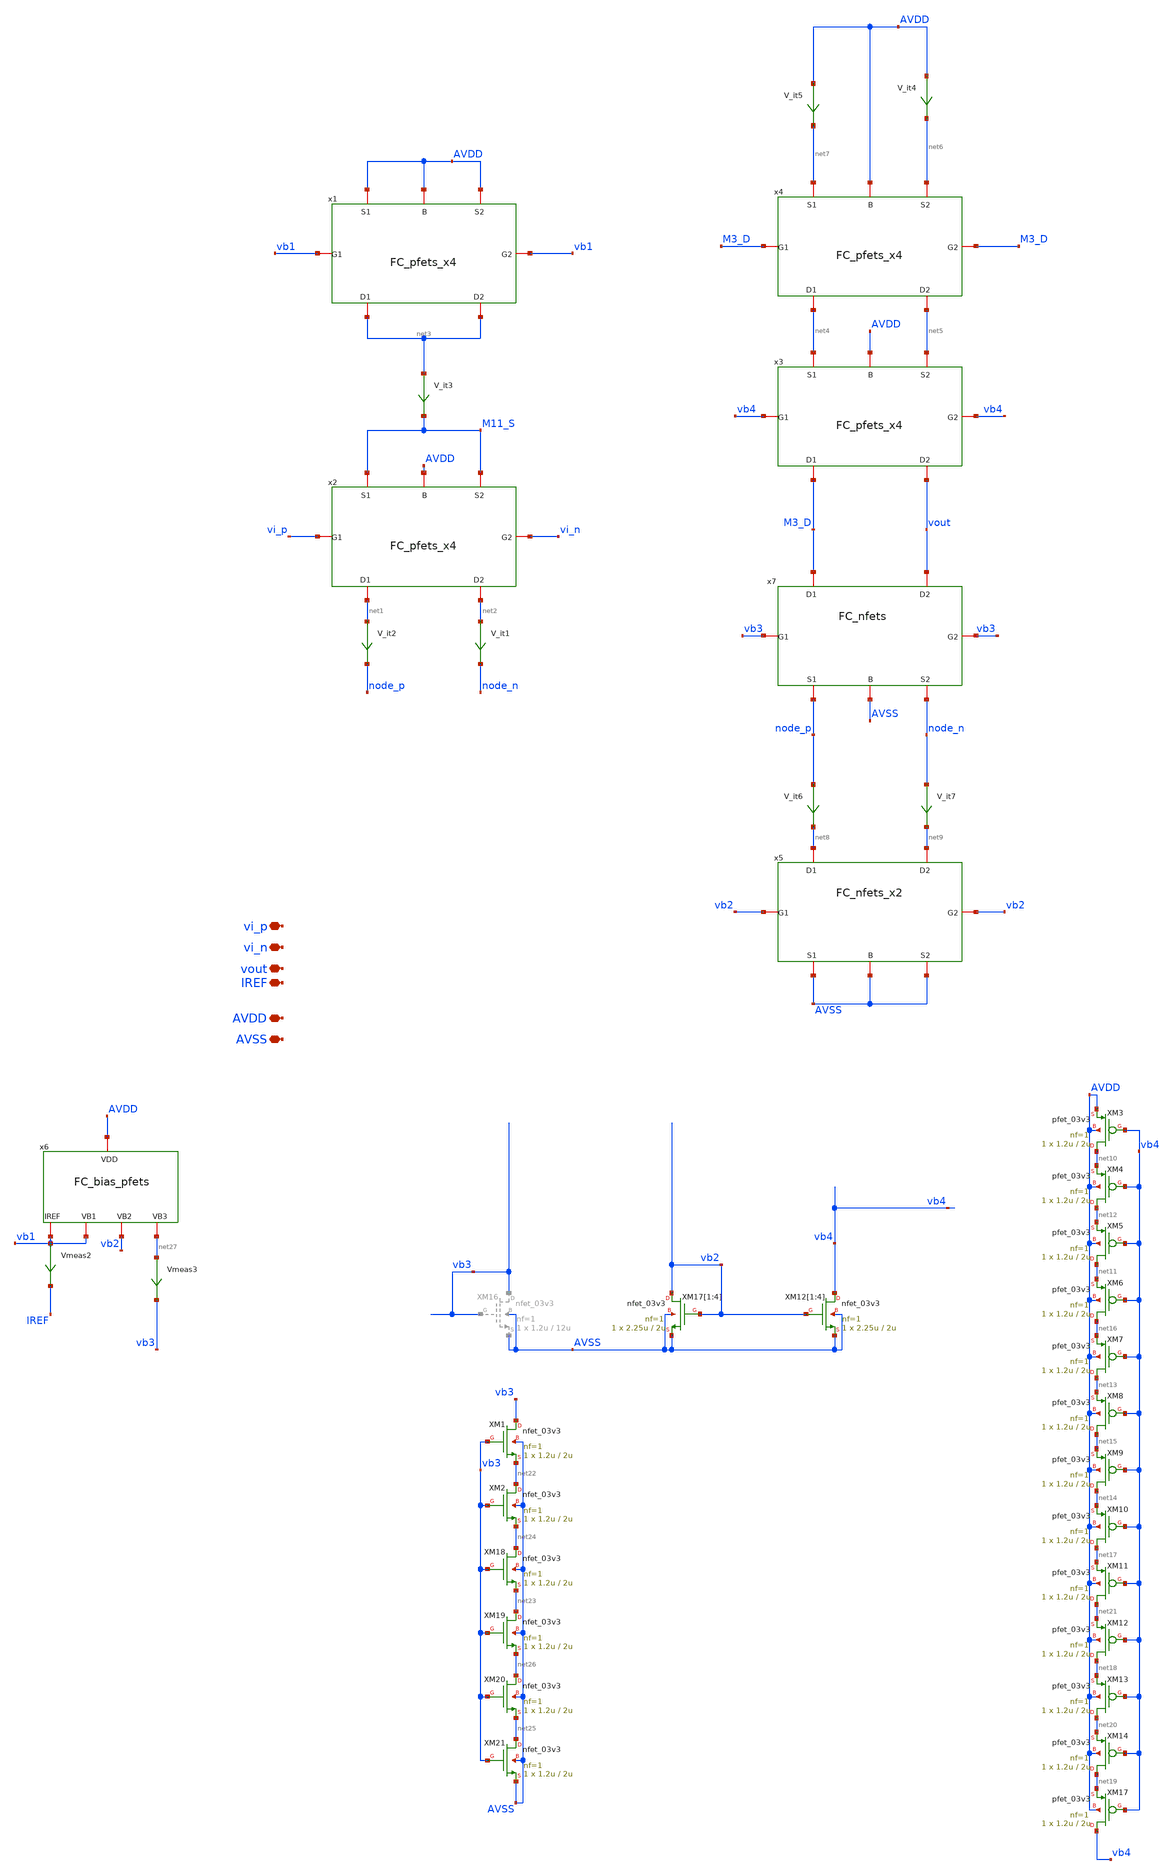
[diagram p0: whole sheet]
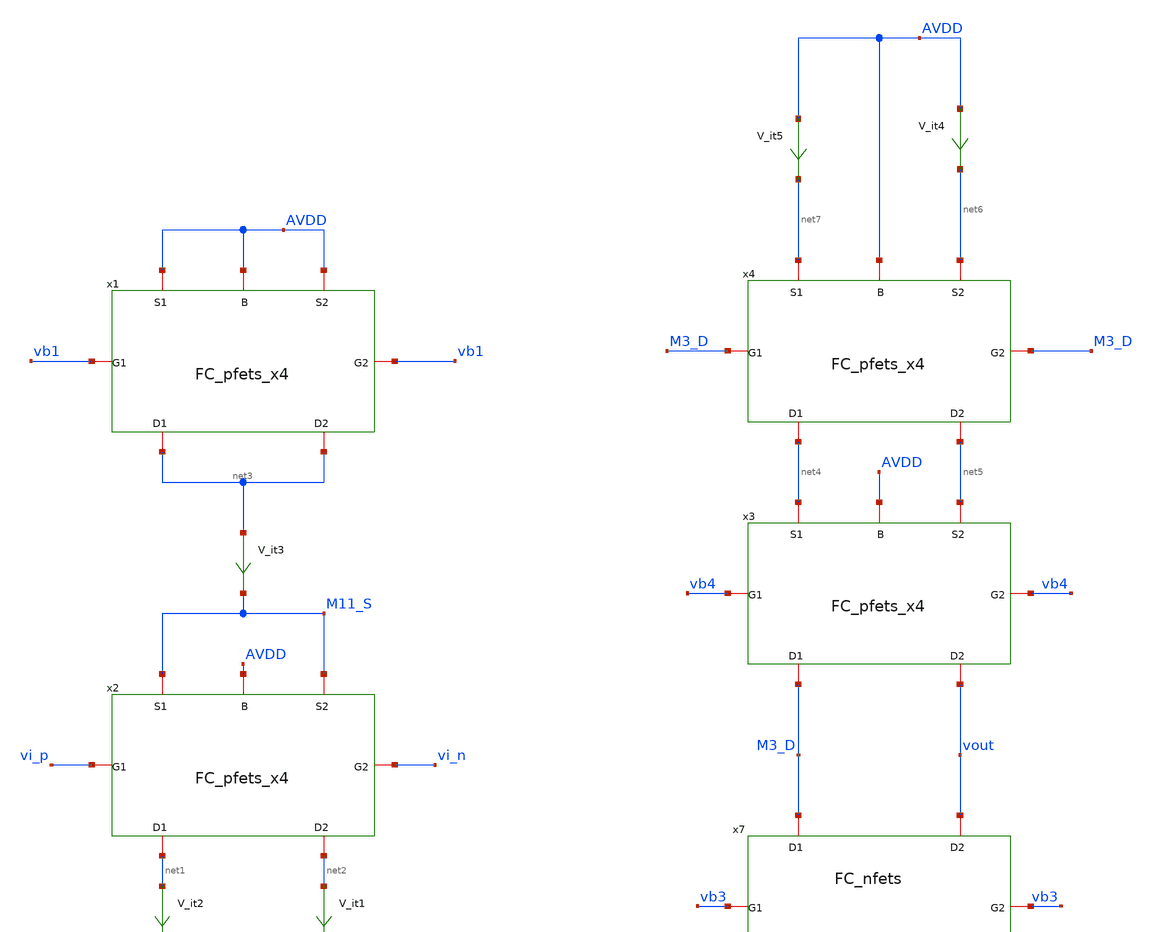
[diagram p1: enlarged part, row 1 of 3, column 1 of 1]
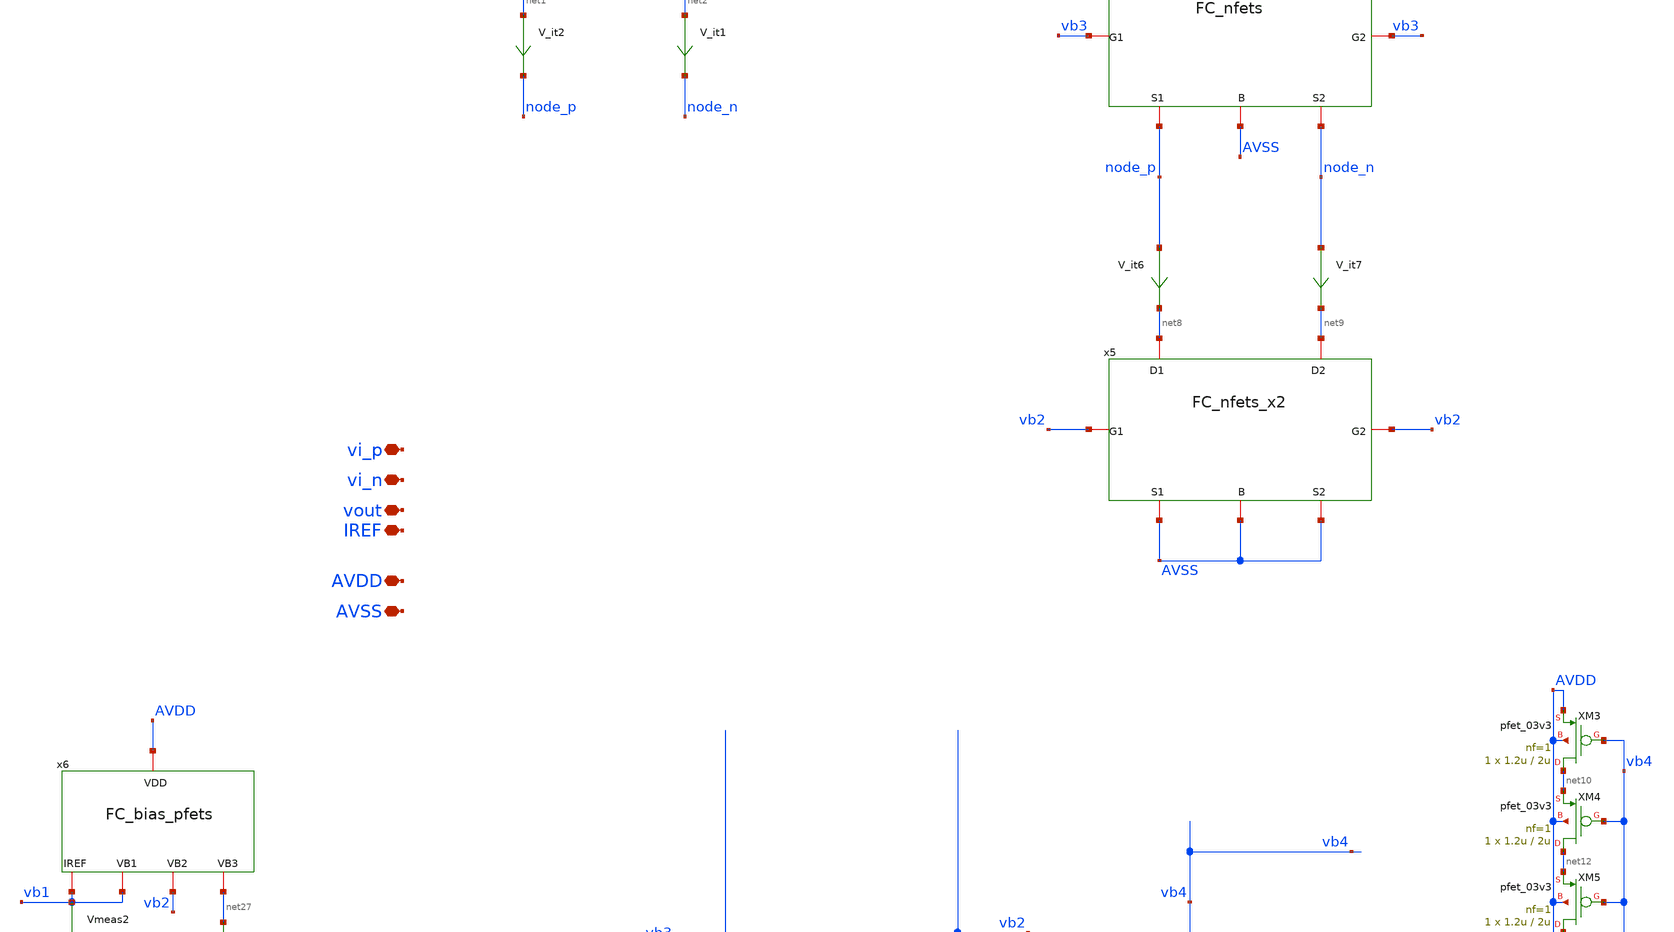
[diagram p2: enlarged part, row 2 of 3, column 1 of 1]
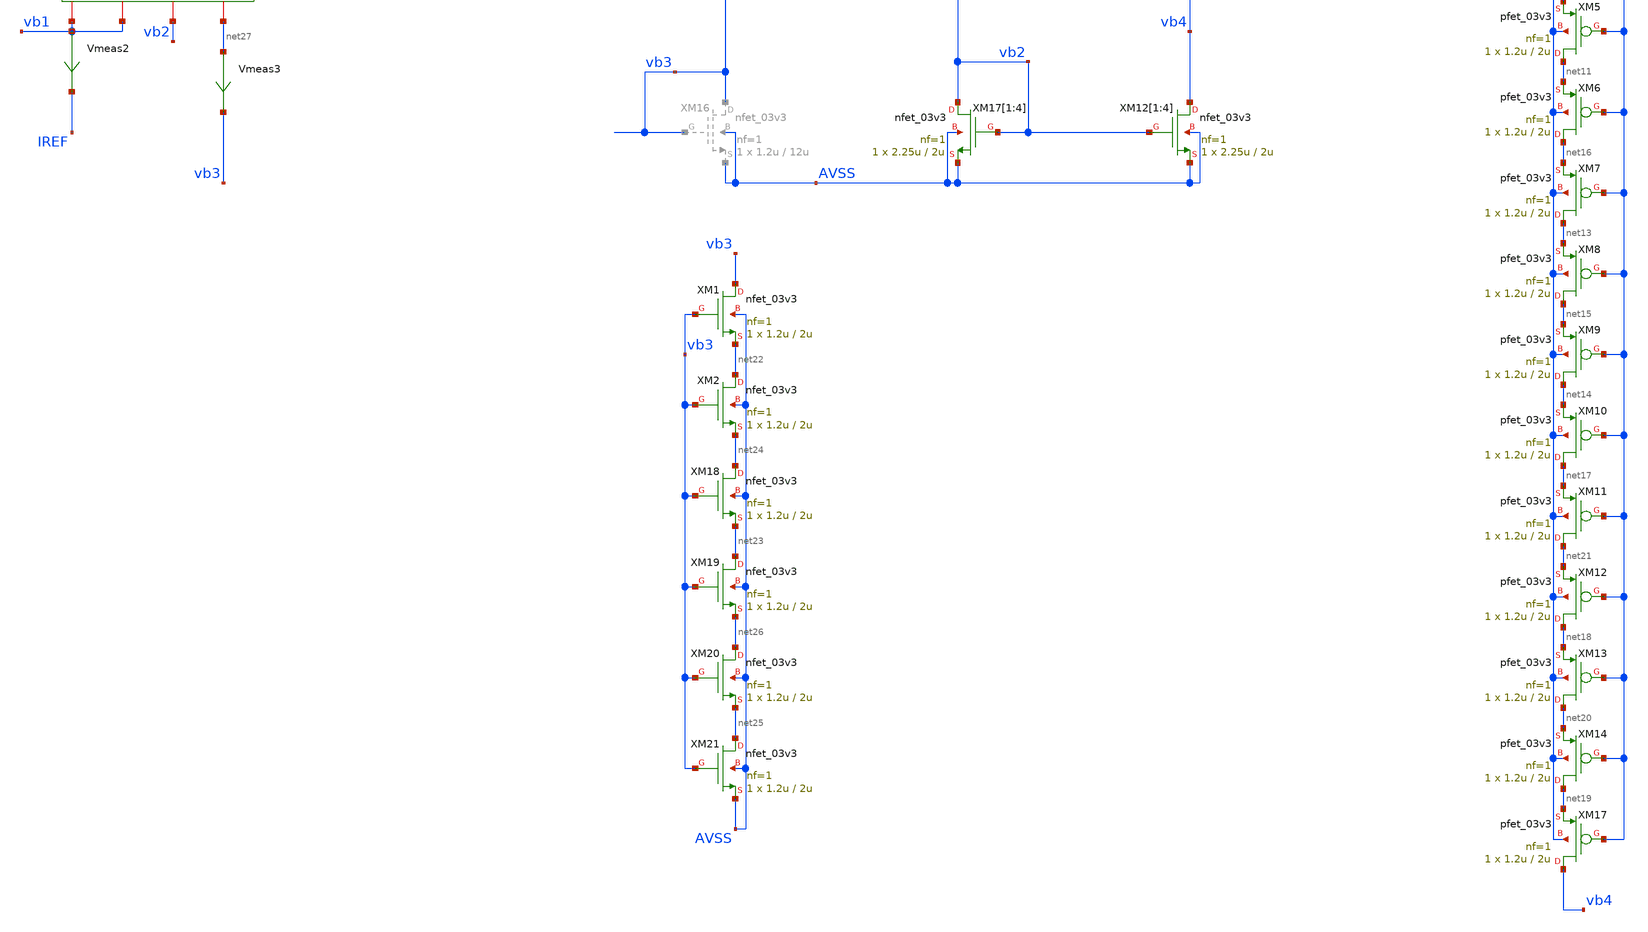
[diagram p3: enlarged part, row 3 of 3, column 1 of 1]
** sch_path: TIA_Filter/Folded/FoldedCascode.sch
**.subckt FoldedCascode AVDD AVSS vout vi_p vi_n IREF
*.iopin AVDD
*.iopin AVSS
*.iopin vout
*.iopin vi_p
*.iopin vi_n
*.iopin IREF
XM17[1] vb2 vb2 AVSS AVSS nfet_03v3 L=2u W=2.25u nf=1 ad='int((nf+1)/2) * W/nf * 0.18u' as='int((nf+2)/2) * W/nf * 0.18u'
+ pd='2*int((nf+1)/2) * (W/nf + 0.18u)' ps='2*int((nf+2)/2) * (W/nf + 0.18u)' nrd='0.18u / W' nrs='0.18u / W'
+ sa=0 sb=0 sd=0 m=1
XM17[2] vb2 vb2 AVSS AVSS nfet_03v3 L=2u W=2.25u nf=1 ad='int((nf+1)/2) * W/nf * 0.18u' as='int((nf+2)/2) * W/nf * 0.18u'
+ pd='2*int((nf+1)/2) * (W/nf + 0.18u)' ps='2*int((nf+2)/2) * (W/nf + 0.18u)' nrd='0.18u / W' nrs='0.18u / W'
+ sa=0 sb=0 sd=0 m=1
XM17[3] vb2 vb2 AVSS AVSS nfet_03v3 L=2u W=2.25u nf=1 ad='int((nf+1)/2) * W/nf * 0.18u' as='int((nf+2)/2) * W/nf * 0.18u'
+ pd='2*int((nf+1)/2) * (W/nf + 0.18u)' ps='2*int((nf+2)/2) * (W/nf + 0.18u)' nrd='0.18u / W' nrs='0.18u / W'
+ sa=0 sb=0 sd=0 m=1
XM17[4] vb2 vb2 AVSS AVSS nfet_03v3 L=2u W=2.25u nf=1 ad='int((nf+1)/2) * W/nf * 0.18u' as='int((nf+2)/2) * W/nf * 0.18u'
+ pd='2*int((nf+1)/2) * (W/nf + 0.18u)' ps='2*int((nf+2)/2) * (W/nf + 0.18u)' nrd='0.18u / W' nrs='0.18u / W'
+ sa=0 sb=0 sd=0 m=1
XM12[1] vb4 vb2 AVSS AVSS nfet_03v3 L=2u W=2.25u nf=1 ad='int((nf+1)/2) * W/nf * 0.18u' as='int((nf+2)/2) * W/nf * 0.18u'
+ pd='2*int((nf+1)/2) * (W/nf + 0.18u)' ps='2*int((nf+2)/2) * (W/nf + 0.18u)' nrd='0.18u / W' nrs='0.18u / W'
+ sa=0 sb=0 sd=0 m=1
XM12[2] vb4 vb2 AVSS AVSS nfet_03v3 L=2u W=2.25u nf=1 ad='int((nf+1)/2) * W/nf * 0.18u' as='int((nf+2)/2) * W/nf * 0.18u'
+ pd='2*int((nf+1)/2) * (W/nf + 0.18u)' ps='2*int((nf+2)/2) * (W/nf + 0.18u)' nrd='0.18u / W' nrs='0.18u / W'
+ sa=0 sb=0 sd=0 m=1
XM12[3] vb4 vb2 AVSS AVSS nfet_03v3 L=2u W=2.25u nf=1 ad='int((nf+1)/2) * W/nf * 0.18u' as='int((nf+2)/2) * W/nf * 0.18u'
+ pd='2*int((nf+1)/2) * (W/nf + 0.18u)' ps='2*int((nf+2)/2) * (W/nf + 0.18u)' nrd='0.18u / W' nrs='0.18u / W'
+ sa=0 sb=0 sd=0 m=1
XM12[4] vb4 vb2 AVSS AVSS nfet_03v3 L=2u W=2.25u nf=1 ad='int((nf+1)/2) * W/nf * 0.18u' as='int((nf+2)/2) * W/nf * 0.18u'
+ pd='2*int((nf+1)/2) * (W/nf + 0.18u)' ps='2*int((nf+2)/2) * (W/nf + 0.18u)' nrd='0.18u / W' nrs='0.18u / W'
+ sa=0 sb=0 sd=0 m=1
V_it1 net2 node_n 0
.save i(v_it1)
V_it2 net1 node_p 0
.save i(v_it2)
V_it3 net3 M11_S 0
.save i(v_it3)
V_it4 AVDD net6 0
.save i(v_it4)
V_it5 AVDD net7 0
.save i(v_it5)
V_it6 node_p net8 0
.save i(v_it6)
V_it7 node_n net9 0
.save i(v_it7)
x7 node_p node_n M3_D vout vb3 vb3 AVSS FC_nfets
x5 AVSS AVSS net8 net9 vb2 vb2 AVSS FC_nfets_x2
x1 AVDD AVDD net3 net3 vb1 vb1 AVDD FC_pfets_x4
x2 M11_S M11_S net1 net2 vi_p vi_n AVDD FC_pfets_x4
x3 net4 net5 M3_D vout vb4 vb4 AVDD FC_pfets_x4
x4 net7 net6 net4 net5 M3_D M3_D AVDD FC_pfets_x4
XM3 net10 vb4 AVDD AVDD pfet_03v3 L=2u W=1.2u nf=1 ad='int((nf+1)/2) * W/nf * 0.18u' as='int((nf+2)/2) * W/nf * 0.18u'
+ pd='2*int((nf+1)/2) * (W/nf + 0.18u)' ps='2*int((nf+2)/2) * (W/nf + 0.18u)' nrd='0.18u / W' nrs='0.18u / W'
+ sa=0 sb=0 sd=0 m=1
XM4 net12 vb4 net10 AVDD pfet_03v3 L=2u W=1.2u nf=1 ad='int((nf+1)/2) * W/nf * 0.18u' as='int((nf+2)/2) * W/nf * 0.18u'
+ pd='2*int((nf+1)/2) * (W/nf + 0.18u)' ps='2*int((nf+2)/2) * (W/nf + 0.18u)' nrd='0.18u / W' nrs='0.18u / W'
+ sa=0 sb=0 sd=0 m=1
XM5 net11 vb4 net12 AVDD pfet_03v3 L=2u W=1.2u nf=1 ad='int((nf+1)/2) * W/nf * 0.18u' as='int((nf+2)/2) * W/nf * 0.18u'
+ pd='2*int((nf+1)/2) * (W/nf + 0.18u)' ps='2*int((nf+2)/2) * (W/nf + 0.18u)' nrd='0.18u / W' nrs='0.18u / W'
+ sa=0 sb=0 sd=0 m=1
XM6 net16 vb4 net11 AVDD pfet_03v3 L=2u W=1.2u nf=1 ad='int((nf+1)/2) * W/nf * 0.18u' as='int((nf+2)/2) * W/nf * 0.18u'
+ pd='2*int((nf+1)/2) * (W/nf + 0.18u)' ps='2*int((nf+2)/2) * (W/nf + 0.18u)' nrd='0.18u / W' nrs='0.18u / W'
+ sa=0 sb=0 sd=0 m=1
XM7 net13 vb4 net16 AVDD pfet_03v3 L=2u W=1.2u nf=1 ad='int((nf+1)/2) * W/nf * 0.18u' as='int((nf+2)/2) * W/nf * 0.18u'
+ pd='2*int((nf+1)/2) * (W/nf + 0.18u)' ps='2*int((nf+2)/2) * (W/nf + 0.18u)' nrd='0.18u / W' nrs='0.18u / W'
+ sa=0 sb=0 sd=0 m=1
XM8 net15 vb4 net13 AVDD pfet_03v3 L=2u W=1.2u nf=1 ad='int((nf+1)/2) * W/nf * 0.18u' as='int((nf+2)/2) * W/nf * 0.18u'
+ pd='2*int((nf+1)/2) * (W/nf + 0.18u)' ps='2*int((nf+2)/2) * (W/nf + 0.18u)' nrd='0.18u / W' nrs='0.18u / W'
+ sa=0 sb=0 sd=0 m=1
XM9 net14 vb4 net15 AVDD pfet_03v3 L=2u W=1.2u nf=1 ad='int((nf+1)/2) * W/nf * 0.18u' as='int((nf+2)/2) * W/nf * 0.18u'
+ pd='2*int((nf+1)/2) * (W/nf + 0.18u)' ps='2*int((nf+2)/2) * (W/nf + 0.18u)' nrd='0.18u / W' nrs='0.18u / W'
+ sa=0 sb=0 sd=0 m=1
XM10 net17 vb4 net14 AVDD pfet_03v3 L=2u W=1.2u nf=1 ad='int((nf+1)/2) * W/nf * 0.18u' as='int((nf+2)/2) * W/nf * 0.18u'
+ pd='2*int((nf+1)/2) * (W/nf + 0.18u)' ps='2*int((nf+2)/2) * (W/nf + 0.18u)' nrd='0.18u / W' nrs='0.18u / W'
+ sa=0 sb=0 sd=0 m=1
XM11 net21 vb4 net17 AVDD pfet_03v3 L=2u W=1.2u nf=1 ad='int((nf+1)/2) * W/nf * 0.18u' as='int((nf+2)/2) * W/nf * 0.18u'
+ pd='2*int((nf+1)/2) * (W/nf + 0.18u)' ps='2*int((nf+2)/2) * (W/nf + 0.18u)' nrd='0.18u / W' nrs='0.18u / W'
+ sa=0 sb=0 sd=0 m=1
XM12 net18 vb4 net21 AVDD pfet_03v3 L=2u W=1.2u nf=1 ad='int((nf+1)/2) * W/nf * 0.18u' as='int((nf+2)/2) * W/nf * 0.18u'
+ pd='2*int((nf+1)/2) * (W/nf + 0.18u)' ps='2*int((nf+2)/2) * (W/nf + 0.18u)' nrd='0.18u / W' nrs='0.18u / W'
+ sa=0 sb=0 sd=0 m=1
XM13 net20 vb4 net18 AVDD pfet_03v3 L=2u W=1.2u nf=1 ad='int((nf+1)/2) * W/nf * 0.18u' as='int((nf+2)/2) * W/nf * 0.18u'
+ pd='2*int((nf+1)/2) * (W/nf + 0.18u)' ps='2*int((nf+2)/2) * (W/nf + 0.18u)' nrd='0.18u / W' nrs='0.18u / W'
+ sa=0 sb=0 sd=0 m=1
XM14 net19 vb4 net20 AVDD pfet_03v3 L=2u W=1.2u nf=1 ad='int((nf+1)/2) * W/nf * 0.18u' as='int((nf+2)/2) * W/nf * 0.18u'
+ pd='2*int((nf+1)/2) * (W/nf + 0.18u)' ps='2*int((nf+2)/2) * (W/nf + 0.18u)' nrd='0.18u / W' nrs='0.18u / W'
+ sa=0 sb=0 sd=0 m=1
XM17 vb4 vb4 net19 AVDD pfet_03v3 L=2u W=1.2u nf=1 ad='int((nf+1)/2) * W/nf * 0.18u' as='int((nf+2)/2) * W/nf * 0.18u'
+ pd='2*int((nf+1)/2) * (W/nf + 0.18u)' ps='2*int((nf+2)/2) * (W/nf + 0.18u)' nrd='0.18u / W' nrs='0.18u / W'
+ sa=0 sb=0 sd=0 m=1
XM1 vb3 vb3 net22 AVSS nfet_03v3 L=2u W=1.2u nf=1 ad='int((nf+1)/2) * W/nf * 0.18u' as='int((nf+2)/2) * W/nf * 0.18u'
+ pd='2*int((nf+1)/2) * (W/nf + 0.18u)' ps='2*int((nf+2)/2) * (W/nf + 0.18u)' nrd='0.18u / W' nrs='0.18u / W'
+ sa=0 sb=0 sd=0 m=1
XM2 net22 vb3 net24 AVSS nfet_03v3 L=2u W=1.2u nf=1 ad='int((nf+1)/2) * W/nf * 0.18u' as='int((nf+2)/2) * W/nf * 0.18u'
+ pd='2*int((nf+1)/2) * (W/nf + 0.18u)' ps='2*int((nf+2)/2) * (W/nf + 0.18u)' nrd='0.18u / W' nrs='0.18u / W'
+ sa=0 sb=0 sd=0 m=1
XM18 net24 vb3 net23 AVSS nfet_03v3 L=2u W=1.2u nf=1 ad='int((nf+1)/2) * W/nf * 0.18u' as='int((nf+2)/2) * W/nf * 0.18u'
+ pd='2*int((nf+1)/2) * (W/nf + 0.18u)' ps='2*int((nf+2)/2) * (W/nf + 0.18u)' nrd='0.18u / W' nrs='0.18u / W'
+ sa=0 sb=0 sd=0 m=1
XM19 net23 vb3 net26 AVSS nfet_03v3 L=2u W=1.2u nf=1 ad='int((nf+1)/2) * W/nf * 0.18u' as='int((nf+2)/2) * W/nf * 0.18u'
+ pd='2*int((nf+1)/2) * (W/nf + 0.18u)' ps='2*int((nf+2)/2) * (W/nf + 0.18u)' nrd='0.18u / W' nrs='0.18u / W'
+ sa=0 sb=0 sd=0 m=1
XM20 net26 vb3 net25 AVSS nfet_03v3 L=2u W=1.2u nf=1 ad='int((nf+1)/2) * W/nf * 0.18u' as='int((nf+2)/2) * W/nf * 0.18u'
+ pd='2*int((nf+1)/2) * (W/nf + 0.18u)' ps='2*int((nf+2)/2) * (W/nf + 0.18u)' nrd='0.18u / W' nrs='0.18u / W'
+ sa=0 sb=0 sd=0 m=1
XM21 net25 vb3 AVSS AVSS nfet_03v3 L=2u W=1.2u nf=1 ad='int((nf+1)/2) * W/nf * 0.18u' as='int((nf+2)/2) * W/nf * 0.18u'
+ pd='2*int((nf+1)/2) * (W/nf + 0.18u)' ps='2*int((nf+2)/2) * (W/nf + 0.18u)' nrd='0.18u / W' nrs='0.18u / W'
+ sa=0 sb=0 sd=0 m=1
Vmeas2 vb1 IREF 0
.save i(vmeas2)
Vmeas3 net27 vb3 0
.save i(vmeas3)
x6 vb1 vb2 net27 vb1 AVDD FC_bias_pfets
**.ends
.end
